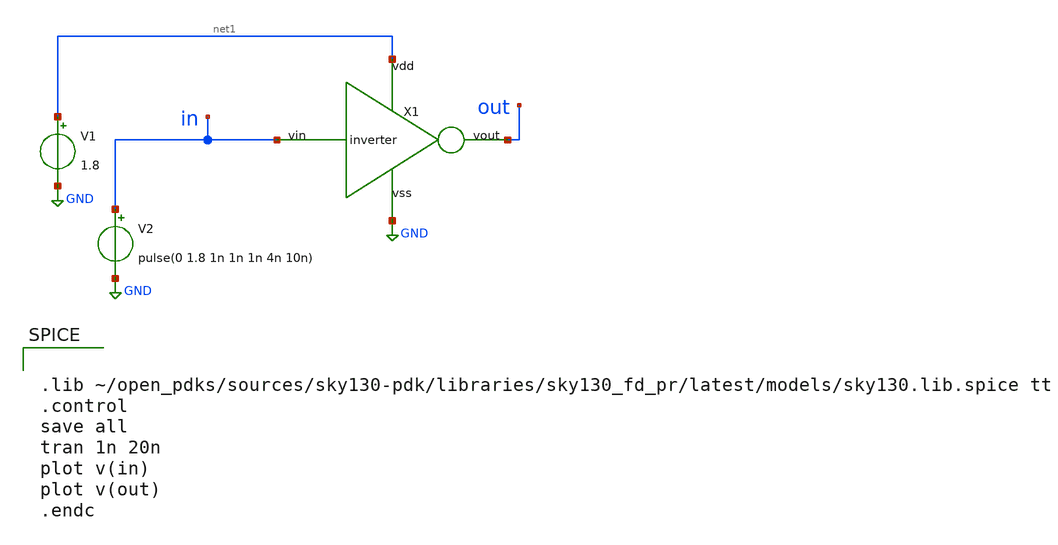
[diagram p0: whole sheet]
** sch_path: Week 0/xschem/inverter_tb.sch
**.subckt inverter_tb
X1 in out net1 GND inverter
V1 net1 GND 1.8
V2 in GND pulse(0 1.8 1n 1n 1n 4n 10n)
**** begin user architecture code


.lib ~/open_pdks/sources/sky130-pdk/libraries/sky130_fd_pr/latest/models/sky130.lib.spice tt
.control
save all
tran 1n 20n
plot v(in)
plot v(out)
.endc

**** end user architecture code
**.ends

* expanding   symbol:  inverter.sym # of pins=4
** sym_path: Week 0/xschem/inverter.sym
** sch_path: Week 0/xschem/inverter.sch
.subckt inverter vin vout vdd vss
*.ipin vin
*.opin vout
*.iopin vdd
*.iopin vss
XM2 vout vin vss vss sky130_fd_pr__nfet_01v8 L=0.15 W=4.2 nf=2 ad='int((nf+1)/2) * W/nf * 0.29' as='int((nf+2)/2) * W/nf * 0.29'
+ pd='2*int((nf+1)/2) * (W/nf + 0.29)' ps='2*int((nf+2)/2) * (W/nf + 0.29)' nrd='0.29 / W' nrs='0.29 / W'
+ sa=0 sb=0 sd=0 mult=1 m=1
XM3 vout vin vdd VDD sky130_fd_pr__pfet_01v8 L=0.15 W=8.4 nf=2 ad='int((nf+1)/2) * W/nf * 0.29' as='int((nf+2)/2) * W/nf * 0.29'
+ pd='2*int((nf+1)/2) * (W/nf + 0.29)' ps='2*int((nf+2)/2) * (W/nf + 0.29)' nrd='0.29 / W' nrs='0.29 / W'
+ sa=0 sb=0 sd=0 mult=1 m=1
.ends

.GLOBAL GND
.end
